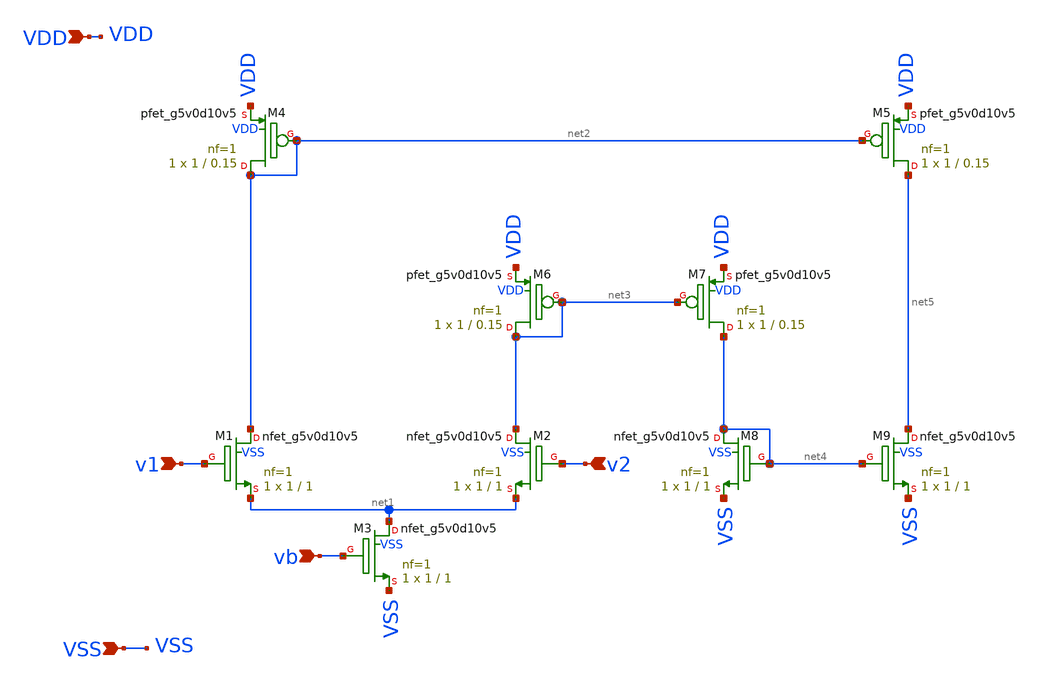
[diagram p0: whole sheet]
** sch_path: xschem/vout_driver.sch
**.subckt vout_driver v1 v2 vb VDD VSS
*.ipin v1
*.ipin v2
*.ipin vb
*.ipin VDD
*.ipin VSS
XM1 net2 v1 net1 VSS sky130_fd_pr__nfet_g5v0d10v5 L=1 W=1 nf=1 ad='int((nf+1)/2) * W/nf * 0.29' as='int((nf+2)/2) * W/nf * 0.29'
+ pd='2*int((nf+1)/2) * (W/nf + 0.29)' ps='2*int((nf+2)/2) * (W/nf + 0.29)' nrd='0.29 / W' nrs='0.29 / W'
+ sa=0 sb=0 sd=0 mult=1 m=1
XM2 net3 v2 net1 VSS sky130_fd_pr__nfet_g5v0d10v5 L=1 W=1 nf=1 ad='int((nf+1)/2) * W/nf * 0.29' as='int((nf+2)/2) * W/nf * 0.29'
+ pd='2*int((nf+1)/2) * (W/nf + 0.29)' ps='2*int((nf+2)/2) * (W/nf + 0.29)' nrd='0.29 / W' nrs='0.29 / W'
+ sa=0 sb=0 sd=0 mult=1 m=1
XM3 net1 vb VSS VSS sky130_fd_pr__nfet_g5v0d10v5 L=1 W=1 nf=1 ad='int((nf+1)/2) * W/nf * 0.29' as='int((nf+2)/2) * W/nf * 0.29'
+ pd='2*int((nf+1)/2) * (W/nf + 0.29)' ps='2*int((nf+2)/2) * (W/nf + 0.29)' nrd='0.29 / W' nrs='0.29 / W'
+ sa=0 sb=0 sd=0 mult=1 m=1
XM4 net2 net2 VDD VDD sky130_fd_pr__pfet_g5v0d10v5 L=0.15 W=1 nf=1 ad='int((nf+1)/2) * W/nf * 0.29' as='int((nf+2)/2) * W/nf * 0.29'
+ pd='2*int((nf+1)/2) * (W/nf + 0.29)' ps='2*int((nf+2)/2) * (W/nf + 0.29)' nrd='0.29 / W' nrs='0.29 / W'
+ sa=0 sb=0 sd=0 mult=1 m=1
XM5 net5 net2 VDD VDD sky130_fd_pr__pfet_g5v0d10v5 L=0.15 W=1 nf=1 ad='int((nf+1)/2) * W/nf * 0.29' as='int((nf+2)/2) * W/nf * 0.29'
+ pd='2*int((nf+1)/2) * (W/nf + 0.29)' ps='2*int((nf+2)/2) * (W/nf + 0.29)' nrd='0.29 / W' nrs='0.29 / W'
+ sa=0 sb=0 sd=0 mult=1 m=1
XM6 net3 net3 VDD VDD sky130_fd_pr__pfet_g5v0d10v5 L=0.15 W=1 nf=1 ad='int((nf+1)/2) * W/nf * 0.29' as='int((nf+2)/2) * W/nf * 0.29'
+ pd='2*int((nf+1)/2) * (W/nf + 0.29)' ps='2*int((nf+2)/2) * (W/nf + 0.29)' nrd='0.29 / W' nrs='0.29 / W'
+ sa=0 sb=0 sd=0 mult=1 m=1
XM7 net4 net3 VDD VDD sky130_fd_pr__pfet_g5v0d10v5 L=0.15 W=1 nf=1 ad='int((nf+1)/2) * W/nf * 0.29' as='int((nf+2)/2) * W/nf * 0.29'
+ pd='2*int((nf+1)/2) * (W/nf + 0.29)' ps='2*int((nf+2)/2) * (W/nf + 0.29)' nrd='0.29 / W' nrs='0.29 / W'
+ sa=0 sb=0 sd=0 mult=1 m=1
XM8 net4 net4 VSS VSS sky130_fd_pr__nfet_g5v0d10v5 L=1 W=1 nf=1 ad='int((nf+1)/2) * W/nf * 0.29' as='int((nf+2)/2) * W/nf * 0.29'
+ pd='2*int((nf+1)/2) * (W/nf + 0.29)' ps='2*int((nf+2)/2) * (W/nf + 0.29)' nrd='0.29 / W' nrs='0.29 / W'
+ sa=0 sb=0 sd=0 mult=1 m=1
XM9 net5 net4 VSS VSS sky130_fd_pr__nfet_g5v0d10v5 L=1 W=1 nf=1 ad='int((nf+1)/2) * W/nf * 0.29' as='int((nf+2)/2) * W/nf * 0.29'
+ pd='2*int((nf+1)/2) * (W/nf + 0.29)' ps='2*int((nf+2)/2) * (W/nf + 0.29)' nrd='0.29 / W' nrs='0.29 / W'
+ sa=0 sb=0 sd=0 mult=1 m=1
**.ends
.end
